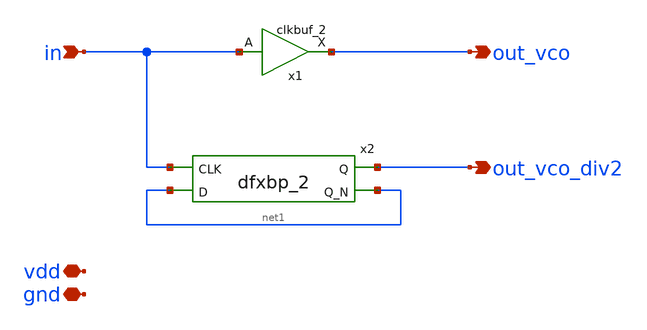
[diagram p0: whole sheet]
** sch_path: xschem/ejf_pll96_outbuf.sch
**.subckt ejf_pll96_outbuf in out_vco_div2 vdd out_vco gnd
*.ipin in
*.opin out_vco_div2
*.iopin vdd
*.opin out_vco
*.iopin gnd
x1 in gnd gnd vdd vdd out_vco sky130_fd_sc_ls__clkbuf_2
x2 in net1 gnd gnd vdd vdd out_vco_div2 net1 sky130_fd_sc_ls__dfxbp_2
**.ends
.end
